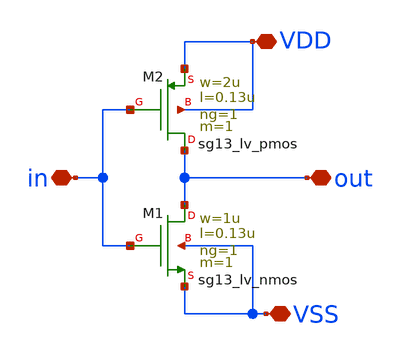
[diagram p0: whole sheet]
** sch_path: xschem/Inverter.sch
**.subckt Inverter VDD VSS in out
*.iopin VDD
*.iopin VSS
*.iopin in
*.iopin out
XM1 out in VSS VSS sg13_lv_nmos w=1u l=0.13u ng=1 m=1 mm_ok=1
XM2 out in VDD VDD sg13_lv_pmos w=2u l=0.13u ng=1 m=1 mm_ok=1
**.ends
.end
